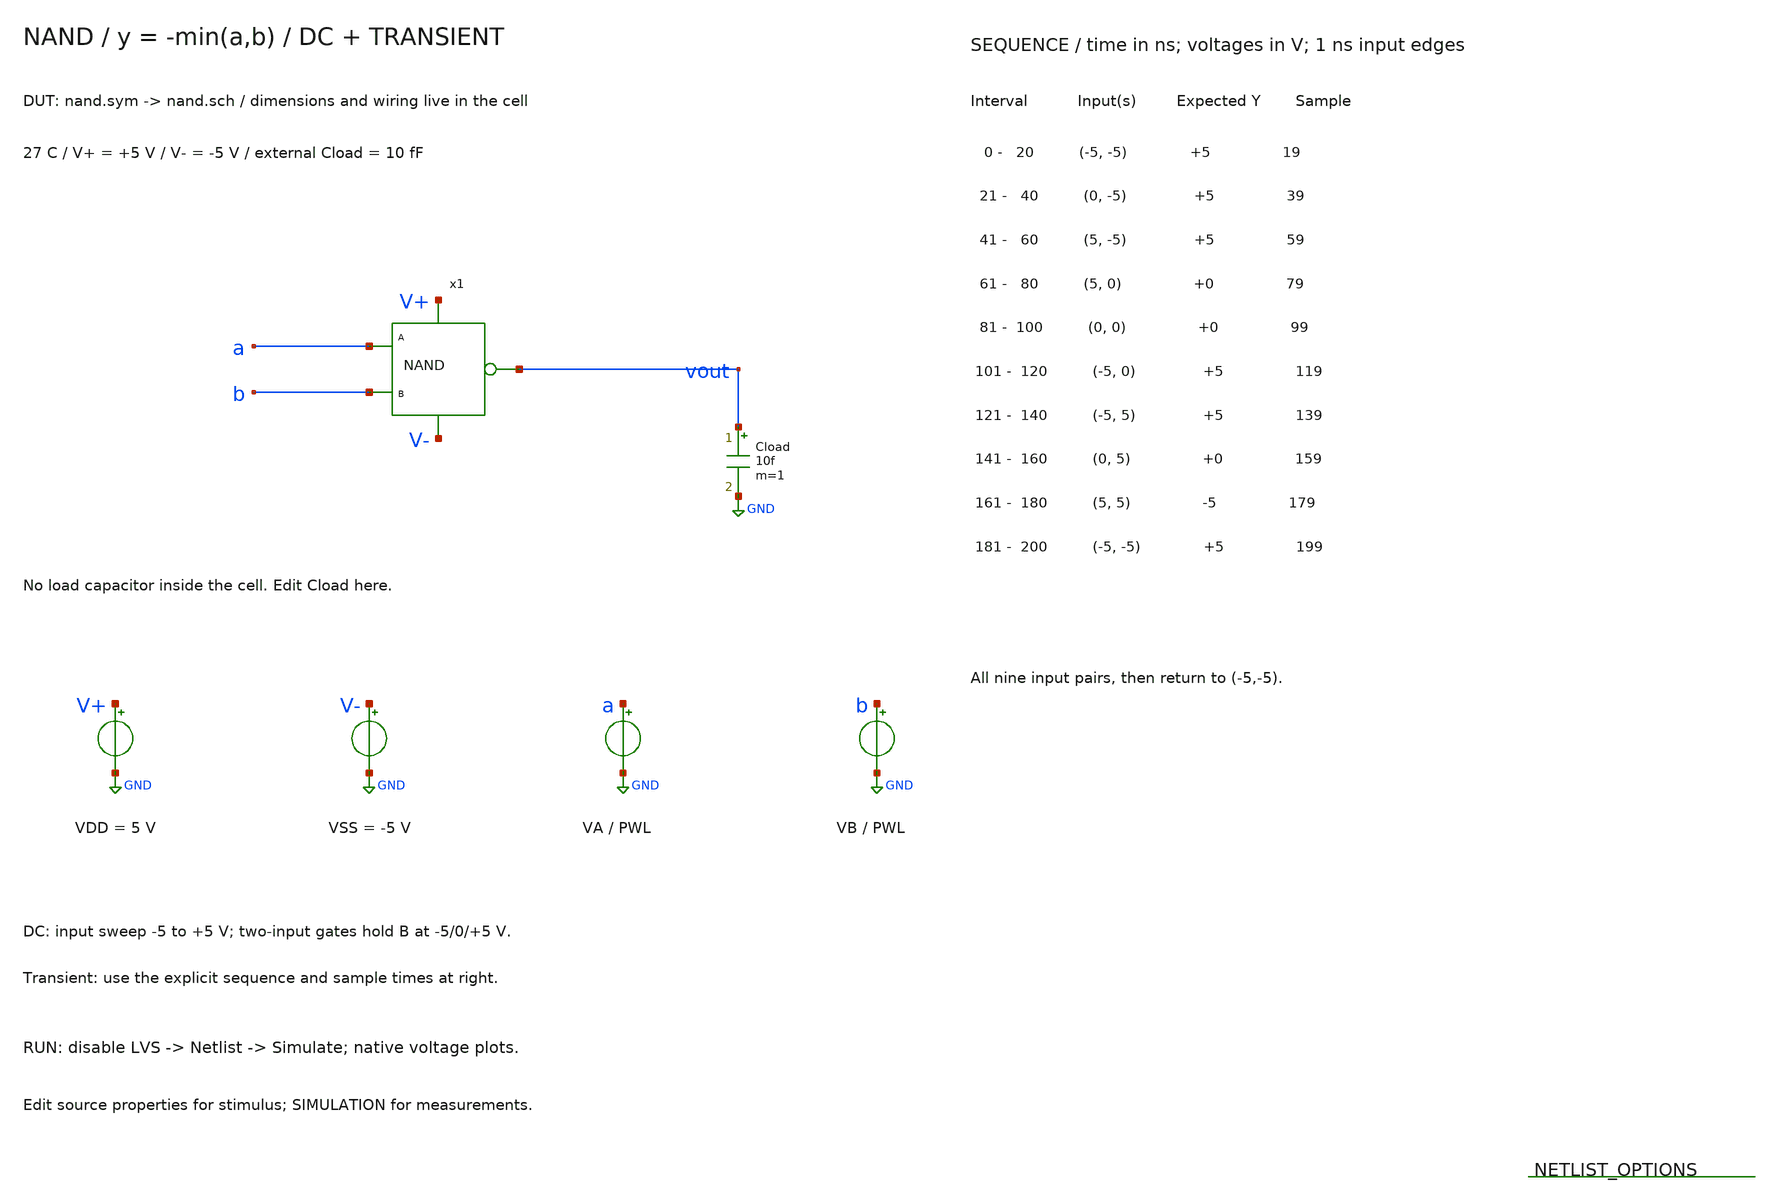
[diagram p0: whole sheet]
** sch_path: member_project/balanced-ternary-logic/PenguinEino/nand_tb.sch
**.subckt nand_tb
x1 a b vout V+ V- nand
Cload vout GND 10f m=1
VDD V+ GND 5
VSS V- GND -5
VA a GND PWL(0 -5 20n -5 21n 0 40n 0 41n 5 60n 5 61n 5 80n 5 81n 0 100n 0 101n -5 120n -5 121n -5
+ 140n -5 141n 0 160n 0 161n 5 180n 5 181n -5 200n -5)
VB b GND PWL(0 -5 20n -5 21n -5 40n -5 41n -5 60n -5 61n 0 80n 0 81n 0 100n 0 101n 0 120n 0 121n 5
+ 140n 5 141n 5 160n 5 161n 5 180n 5 181n -5 200n -5)
**** begin user architecture code
 .include $::LIB/ip62_models

.temp 27
BEXPECTED expected 0 V=-min(v(a),v(b))
BERROR output_error 0 V=v(vout)-v(expected)
.nodeset v(vout)=5 v(x1.net1)=5 v(x1.net2)=-5 v(x1.net3)=-5
.options rshunt=1e12
.control
save all
setplot const
let failures=0
reset
alter VB -5
dc VA -5 5 0.015625
meas dc DC_A_NEG_B_NEG find v(vout) at=-5
meas dc ERR_DC_A_NEG_B_NEG find v(output_error) at=-5
if abs(ERR_DC_A_NEG_B_NEG) > 0.5
let const.failures=const.failures+1
echo FAIL: DC_A_NEG_B_NEG outside expected +/-0.5V
end
meas dc DC_A_ZERO_B_NEG find v(vout) at=0
meas dc ERR_DC_A_ZERO_B_NEG find v(output_error) at=0
if abs(ERR_DC_A_ZERO_B_NEG) > 0.5
let const.failures=const.failures+1
echo FAIL: DC_A_ZERO_B_NEG outside expected +/-0.5V
end
meas dc DC_A_POS_B_NEG find v(vout) at=5
meas dc ERR_DC_A_POS_B_NEG find v(output_error) at=5
if abs(ERR_DC_A_POS_B_NEG) > 0.5
let const.failures=const.failures+1
echo FAIL: DC_A_POS_B_NEG outside expected +/-0.5V
end
plot v(a) v(vout) v(expected) ylimit -5.5 5.5 title 'NAND DC: sweep A, B = -5 V'
reset
alter VB 0
dc VA -5 5 0.015625
meas dc DC_A_NEG_B_ZERO find v(vout) at=-5
meas dc ERR_DC_A_NEG_B_ZERO find v(output_error) at=-5
if abs(ERR_DC_A_NEG_B_ZERO) > 0.5
let const.failures=const.failures+1
echo FAIL: DC_A_NEG_B_ZERO outside expected +/-0.5V
end
meas dc DC_A_ZERO_B_ZERO find v(vout) at=0
meas dc ERR_DC_A_ZERO_B_ZERO find v(output_error) at=0
if abs(ERR_DC_A_ZERO_B_ZERO) > 0.5
let const.failures=const.failures+1
echo FAIL: DC_A_ZERO_B_ZERO outside expected +/-0.5V
end
meas dc DC_A_POS_B_ZERO find v(vout) at=5
meas dc ERR_DC_A_POS_B_ZERO find v(output_error) at=5
if abs(ERR_DC_A_POS_B_ZERO) > 0.5
let const.failures=const.failures+1
echo FAIL: DC_A_POS_B_ZERO outside expected +/-0.5V
end
plot v(a) v(vout) v(expected) ylimit -5.5 5.5 title 'NAND DC: sweep A, B = 0 V'
reset
alter VB 5
dc VA -5 5 0.015625
meas dc DC_A_NEG_B_POS find v(vout) at=-5
meas dc ERR_DC_A_NEG_B_POS find v(output_error) at=-5
if abs(ERR_DC_A_NEG_B_POS) > 0.5
let const.failures=const.failures+1
echo FAIL: DC_A_NEG_B_POS outside expected +/-0.5V
end
meas dc DC_A_ZERO_B_POS find v(vout) at=0
meas dc ERR_DC_A_ZERO_B_POS find v(output_error) at=0
if abs(ERR_DC_A_ZERO_B_POS) > 0.5
let const.failures=const.failures+1
echo FAIL: DC_A_ZERO_B_POS outside expected +/-0.5V
end
meas dc DC_A_POS_B_POS find v(vout) at=5
meas dc ERR_DC_A_POS_B_POS find v(output_error) at=5
if abs(ERR_DC_A_POS_B_POS) > 0.5
let const.failures=const.failures+1
echo FAIL: DC_A_POS_B_POS outside expected +/-0.5V
end
plot v(a) v(vout) v(expected) ylimit -5.5 5.5 title 'NAND DC: sweep A, B = 5 V'
reset
tran 0.05n 200n
meas tran OUT_01 find v(vout) at=19n
meas tran ERR_OUT_01 find v(output_error) at=19n
if abs(ERR_OUT_01) > 0.5
let const.failures=const.failures+1
echo FAIL: OUT_01 outside expected +/-0.5V
end
meas tran OUT_02 find v(vout) at=39n
meas tran ERR_OUT_02 find v(output_error) at=39n
if abs(ERR_OUT_02) > 0.5
let const.failures=const.failures+1
echo FAIL: OUT_02 outside expected +/-0.5V
end
meas tran OUT_03 find v(vout) at=59n
meas tran ERR_OUT_03 find v(output_error) at=59n
if abs(ERR_OUT_03) > 0.5
let const.failures=const.failures+1
echo FAIL: OUT_03 outside expected +/-0.5V
end
meas tran OUT_04 find v(vout) at=79n
meas tran ERR_OUT_04 find v(output_error) at=79n
if abs(ERR_OUT_04) > 0.5
let const.failures=const.failures+1
echo FAIL: OUT_04 outside expected +/-0.5V
end
meas tran OUT_05 find v(vout) at=99n
meas tran ERR_OUT_05 find v(output_error) at=99n
if abs(ERR_OUT_05) > 0.5
let const.failures=const.failures+1
echo FAIL: OUT_05 outside expected +/-0.5V
end
meas tran OUT_06 find v(vout) at=119n
meas tran ERR_OUT_06 find v(output_error) at=119n
if abs(ERR_OUT_06) > 0.5
let const.failures=const.failures+1
echo FAIL: OUT_06 outside expected +/-0.5V
end
meas tran OUT_07 find v(vout) at=139n
meas tran ERR_OUT_07 find v(output_error) at=139n
if abs(ERR_OUT_07) > 0.5
let const.failures=const.failures+1
echo FAIL: OUT_07 outside expected +/-0.5V
end
meas tran OUT_08 find v(vout) at=159n
meas tran ERR_OUT_08 find v(output_error) at=159n
if abs(ERR_OUT_08) > 0.5
let const.failures=const.failures+1
echo FAIL: OUT_08 outside expected +/-0.5V
end
meas tran OUT_09 find v(vout) at=179n
meas tran ERR_OUT_09 find v(output_error) at=179n
if abs(ERR_OUT_09) > 0.5
let const.failures=const.failures+1
echo FAIL: OUT_09 outside expected +/-0.5V
end
meas tran OUT_10 find v(vout) at=199n
meas tran ERR_OUT_10 find v(output_error) at=199n
if abs(ERR_OUT_10) > 0.5
let const.failures=const.failures+1
echo FAIL: OUT_10 outside expected +/-0.5V
end
plot v(a) v(b) v(vout) v(expected) ylimit -5.5 5.5 title 'NAND: A, B and output / all nine input pairs'
if const.failures = 0
echo PASS: all DC and transient samples within expected +/-0.5V
else
echo FAIL: NAND truth-table samples outside tolerance
print const.failures
end
.endc

**** end user architecture code
**.ends

* expanding   symbol:  /home/ishi-kai/balanced-ternary-logic/nand.sym # of pins=5
** sym_path: member_project/balanced-ternary-logic/PenguinEino/nand.sym
** sch_path: member_project/balanced-ternary-logic/PenguinEino/nand.sch
.subckt nand a b vout V+ V-
*.iopin V+
*.ipin a
*.ipin b
*.opin vout
*.iopin V-
XXM1 net1 a V+ V+ PMOS w=24u l=1u nrd=0 nrs=0 m=1
XXM3 net1 b V+ V+ PMOS w=24u l=1u nrd=0 nrs=0 m=1
XR1 net1 vout V+ F_RR w=2.8e-06 l=15e-06 R=1 tc1=0 tc2=0 m=1
XR2 vout net2 V+ F_RR w=2.8e-06 l=15e-06 R=1 tc1=0 tc2=0 m=1
XXM2 net2 a net3 V- NMOS w=16u l=1u nrd=0 nrs=0 m=1
XXM4 net3 b V- V- NMOS w=16u l=1u nrd=0 nrs=0 m=1
.ends

.GLOBAL GND
.end
